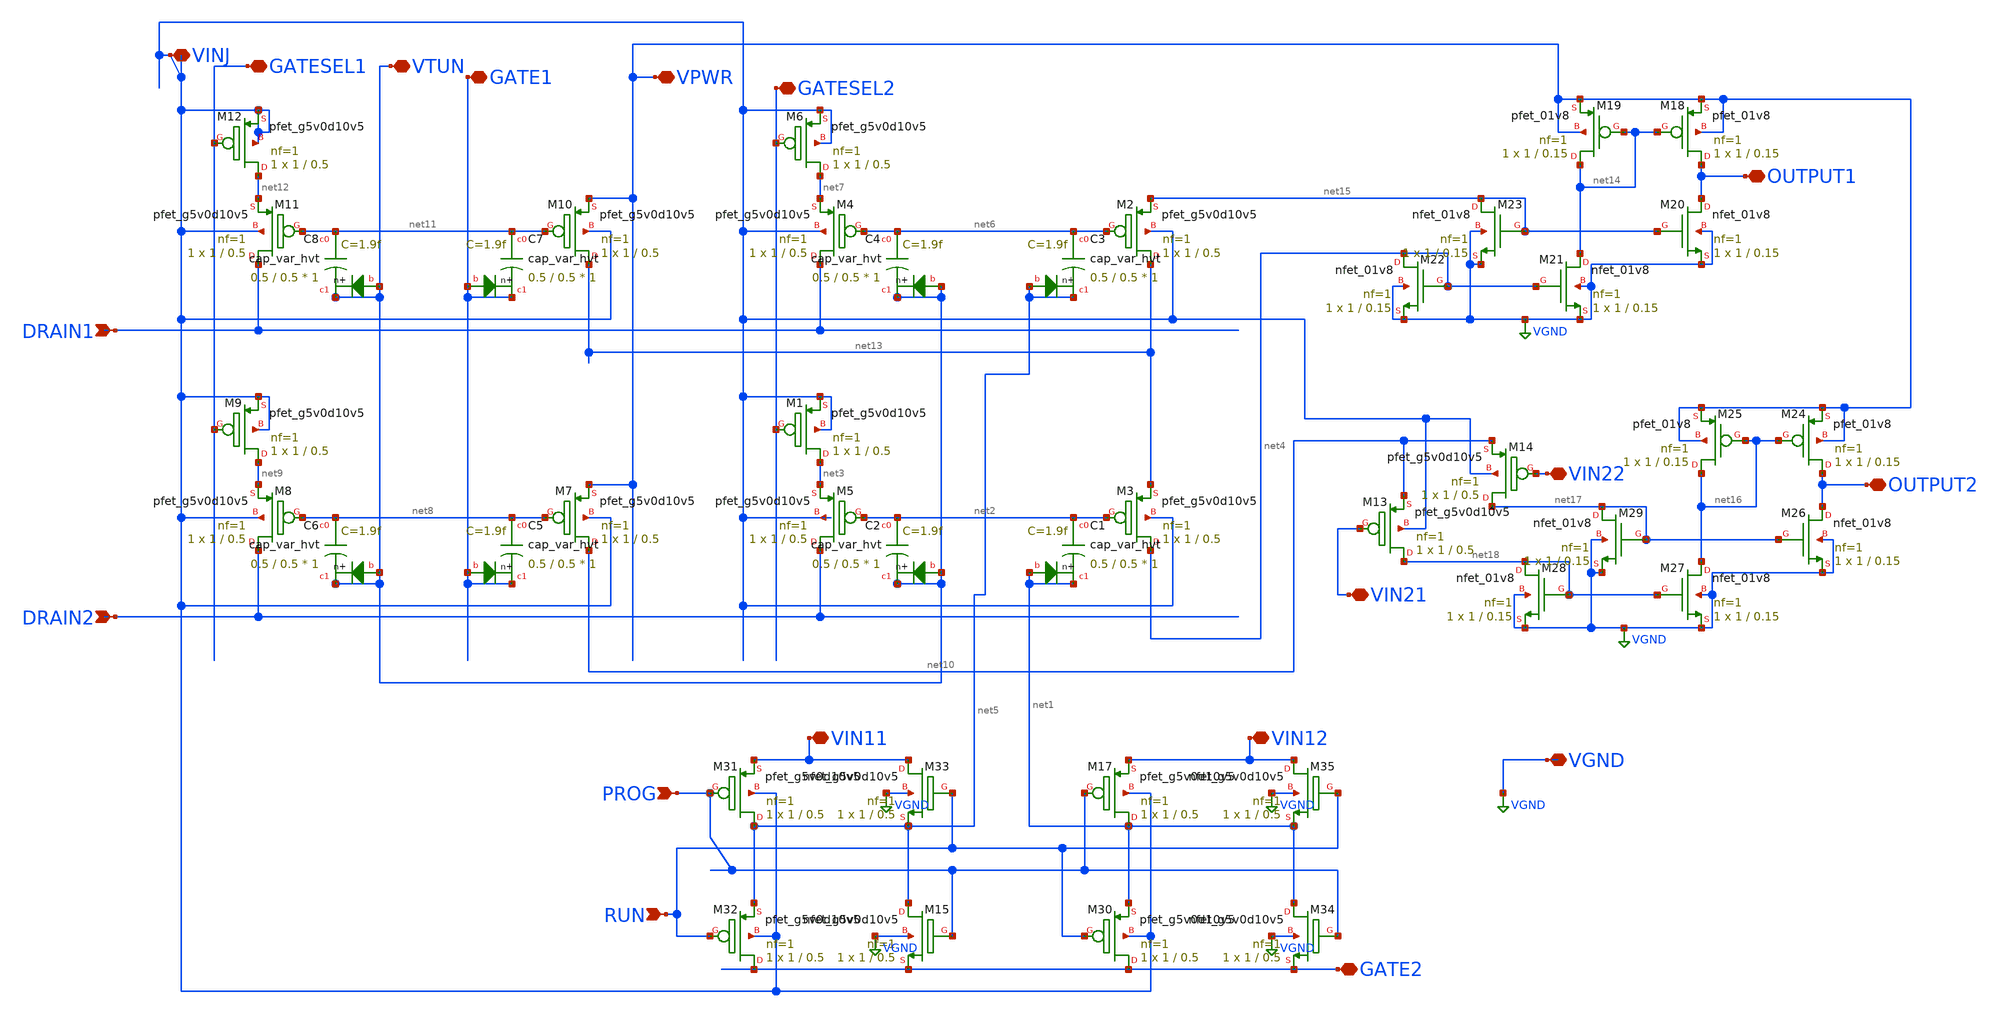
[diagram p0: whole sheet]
** sch_path: libs.ref/sky130_hilas_sc/xschem/sky130_hilas_TA2Cell_1FG_Strong.sch
**.subckt sky130_hilas_TA2Cell_1FG_Strong DRAIN1 DRAIN2 RUN PROG VPWR GATE1 VTUN GATESEL1 VINJ
*+ GATESEL2 GATE2 OUTPUT1 OUTPUT2 VIN11 VIN21 VIN12 VIN22 VGND
*.ipin DRAIN1
*.ipin DRAIN2
*.ipin RUN
*.ipin PROG
*.iopin VPWR
*.iopin GATE1
*.iopin VTUN
*.iopin GATESEL1
*.iopin VINJ
*.iopin GATESEL2
*.iopin GATE2
*.iopin OUTPUT1
*.iopin OUTPUT2
*.iopin VIN11
*.iopin VIN21
*.iopin VIN12
*.iopin VIN22
*.iopin VGND
XM3 net4 net2 net13 VINJ sky130_fd_pr__pfet_g5v0d10v5 L=0.5 W=1 nf=1 ad='int((nf+1)/2) * W/nf * 0.29'
+ as='int((nf+2)/2) * W/nf * 0.29' pd='2*int((nf+1)/2) * (W/nf + 0.29)' ps='2*int((nf+2)/2) * (W/nf + 0.29)'
+ nrd='0.29 / W' nrs='0.29 / W' sa=0 sb=0 sd=0 mult=1 m=1
XC1 net2 net1 net1 sky130_fd_pr__cap_var_hvt W=0.5 L=0.5 VM=1 m=1
XM5 DRAIN2 net2 net3 VINJ sky130_fd_pr__pfet_g5v0d10v5 L=0.5 W=1 nf=1 ad='int((nf+1)/2) * W/nf * 0.29'
+ as='int((nf+2)/2) * W/nf * 0.29' pd='2*int((nf+1)/2) * (W/nf + 0.29)' ps='2*int((nf+2)/2) * (W/nf + 0.29)'
+ nrd='0.29 / W' nrs='0.29 / W' sa=0 sb=0 sd=0 mult=1 m=1
XC2 net2 VTUN VTUN sky130_fd_pr__cap_var_hvt W=0.5 L=0.5 VM=1 m=1
XM1 net3 GATESEL2 VINJ VINJ sky130_fd_pr__pfet_g5v0d10v5 L=0.5 W=1 nf=1 ad='int((nf+1)/2) * W/nf * 0.29'
+ as='int((nf+2)/2) * W/nf * 0.29' pd='2*int((nf+1)/2) * (W/nf + 0.29)' ps='2*int((nf+2)/2) * (W/nf + 0.29)'
+ nrd='0.29 / W' nrs='0.29 / W' sa=0 sb=0 sd=0 mult=1 m=1
XM2 net13 net6 net15 VINJ sky130_fd_pr__pfet_g5v0d10v5 L=0.5 W=1 nf=1 ad='int((nf+1)/2) * W/nf * 0.29'
+ as='int((nf+2)/2) * W/nf * 0.29' pd='2*int((nf+1)/2) * (W/nf + 0.29)' ps='2*int((nf+2)/2) * (W/nf + 0.29)'
+ nrd='0.29 / W' nrs='0.29 / W' sa=0 sb=0 sd=0 mult=1 m=1
XC3 net6 net5 net5 sky130_fd_pr__cap_var_hvt W=0.5 L=0.5 VM=1 m=1
XM4 DRAIN1 net6 net7 VINJ sky130_fd_pr__pfet_g5v0d10v5 L=0.5 W=1 nf=1 ad='int((nf+1)/2) * W/nf * 0.29'
+ as='int((nf+2)/2) * W/nf * 0.29' pd='2*int((nf+1)/2) * (W/nf + 0.29)' ps='2*int((nf+2)/2) * (W/nf + 0.29)'
+ nrd='0.29 / W' nrs='0.29 / W' sa=0 sb=0 sd=0 mult=1 m=1
XC4 net6 VTUN VTUN sky130_fd_pr__cap_var_hvt W=0.5 L=0.5 VM=1 m=1
XM6 net7 GATESEL2 VINJ VINJ sky130_fd_pr__pfet_g5v0d10v5 L=0.5 W=1 nf=1 ad='int((nf+1)/2) * W/nf * 0.29'
+ as='int((nf+2)/2) * W/nf * 0.29' pd='2*int((nf+1)/2) * (W/nf + 0.29)' ps='2*int((nf+2)/2) * (W/nf + 0.29)'
+ nrd='0.29 / W' nrs='0.29 / W' sa=0 sb=0 sd=0 mult=1 m=1
XM7 net10 net8 VPWR VINJ sky130_fd_pr__pfet_g5v0d10v5 L=0.5 W=1 nf=1 ad='int((nf+1)/2) * W/nf * 0.29'
+ as='int((nf+2)/2) * W/nf * 0.29' pd='2*int((nf+1)/2) * (W/nf + 0.29)' ps='2*int((nf+2)/2) * (W/nf + 0.29)'
+ nrd='0.29 / W' nrs='0.29 / W' sa=0 sb=0 sd=0 mult=1 m=1
XC5 net8 GATE1 GATE1 sky130_fd_pr__cap_var_hvt W=0.5 L=0.5 VM=1 m=1
XM8 DRAIN2 net8 net9 VINJ sky130_fd_pr__pfet_g5v0d10v5 L=0.5 W=1 nf=1 ad='int((nf+1)/2) * W/nf * 0.29'
+ as='int((nf+2)/2) * W/nf * 0.29' pd='2*int((nf+1)/2) * (W/nf + 0.29)' ps='2*int((nf+2)/2) * (W/nf + 0.29)'
+ nrd='0.29 / W' nrs='0.29 / W' sa=0 sb=0 sd=0 mult=1 m=1
XC6 net8 VTUN VTUN sky130_fd_pr__cap_var_hvt W=0.5 L=0.5 VM=1 m=1
XM9 net9 GATESEL1 VINJ VINJ sky130_fd_pr__pfet_g5v0d10v5 L=0.5 W=1 nf=1 ad='int((nf+1)/2) * W/nf * 0.29'
+ as='int((nf+2)/2) * W/nf * 0.29' pd='2*int((nf+1)/2) * (W/nf + 0.29)' ps='2*int((nf+2)/2) * (W/nf + 0.29)'
+ nrd='0.29 / W' nrs='0.29 / W' sa=0 sb=0 sd=0 mult=1 m=1
XM10 net13 net11 VPWR VINJ sky130_fd_pr__pfet_g5v0d10v5 L=0.5 W=1 nf=1 ad='int((nf+1)/2) * W/nf * 0.29'
+ as='int((nf+2)/2) * W/nf * 0.29' pd='2*int((nf+1)/2) * (W/nf + 0.29)' ps='2*int((nf+2)/2) * (W/nf + 0.29)'
+ nrd='0.29 / W' nrs='0.29 / W' sa=0 sb=0 sd=0 mult=1 m=1
XC7 net11 GATE1 GATE1 sky130_fd_pr__cap_var_hvt W=0.5 L=0.5 VM=1 m=1
XM11 DRAIN1 net11 net12 VINJ sky130_fd_pr__pfet_g5v0d10v5 L=0.5 W=1 nf=1 ad='int((nf+1)/2) * W/nf * 0.29'
+ as='int((nf+2)/2) * W/nf * 0.29' pd='2*int((nf+1)/2) * (W/nf + 0.29)' ps='2*int((nf+2)/2) * (W/nf + 0.29)'
+ nrd='0.29 / W' nrs='0.29 / W' sa=0 sb=0 sd=0 mult=1 m=1
XC8 net11 VTUN VTUN sky130_fd_pr__cap_var_hvt W=0.5 L=0.5 VM=1 m=1
XM12 net12 GATESEL1 VINJ VINJ sky130_fd_pr__pfet_g5v0d10v5 L=0.5 W=1 nf=1 ad='int((nf+1)/2) * W/nf * 0.29'
+ as='int((nf+2)/2) * W/nf * 0.29' pd='2*int((nf+1)/2) * (W/nf + 0.29)' ps='2*int((nf+2)/2) * (W/nf + 0.29)'
+ nrd='0.29 / W' nrs='0.29 / W' sa=0 sb=0 sd=0 mult=1 m=1
XM15 net5 PROG GATE2 VGND sky130_fd_pr__nfet_g5v0d10v5 L=0.5 W=1 nf=1 ad='int((nf+1)/2) * W/nf * 0.29'
+ as='int((nf+2)/2) * W/nf * 0.29' pd='2*int((nf+1)/2) * (W/nf + 0.29)' ps='2*int((nf+2)/2) * (W/nf + 0.29)'
+ nrd='0.29 / W' nrs='0.29 / W' sa=0 sb=0 sd=0 mult=1 m=1
XM17 net1 PROG VIN12 VINJ sky130_fd_pr__pfet_g5v0d10v5 L=0.5 W=1 nf=1 ad='int((nf+1)/2) * W/nf * 0.29'
+ as='int((nf+2)/2) * W/nf * 0.29' pd='2*int((nf+1)/2) * (W/nf + 0.29)' ps='2*int((nf+2)/2) * (W/nf + 0.29)'
+ nrd='0.29 / W' nrs='0.29 / W' sa=0 sb=0 sd=0 mult=1 m=1
XM18 OUTPUT1 net14 VPWR VPWR sky130_fd_pr__pfet_01v8 L=0.15 W=1 nf=1 ad='int((nf+1)/2) * W/nf * 0.29'
+ as='int((nf+2)/2) * W/nf * 0.29' pd='2*int((nf+1)/2) * (W/nf + 0.29)' ps='2*int((nf+2)/2) * (W/nf + 0.29)'
+ nrd='0.29 / W' nrs='0.29 / W' sa=0 sb=0 sd=0 mult=1 m=1
XM19 net14 net14 VPWR VPWR sky130_fd_pr__pfet_01v8 L=0.15 W=1 nf=1 ad='int((nf+1)/2) * W/nf * 0.29' as='int((nf+2)/2) * W/nf * 0.29'
+ pd='2*int((nf+1)/2) * (W/nf + 0.29)' ps='2*int((nf+2)/2) * (W/nf + 0.29)' nrd='0.29 / W' nrs='0.29 / W'
+ sa=0 sb=0 sd=0 mult=1 m=1
XM20 OUTPUT1 net15 VGND VGND sky130_fd_pr__nfet_01v8 L=0.15 W=1 nf=1 ad='int((nf+1)/2) * W/nf * 0.29'
+ as='int((nf+2)/2) * W/nf * 0.29' pd='2*int((nf+1)/2) * (W/nf + 0.29)' ps='2*int((nf+2)/2) * (W/nf + 0.29)'
+ nrd='0.29 / W' nrs='0.29 / W' sa=0 sb=0 sd=0 mult=1 m=1
XM21 net14 net4 VGND VGND sky130_fd_pr__nfet_01v8 L=0.15 W=1 nf=1 ad='int((nf+1)/2) * W/nf * 0.29' as='int((nf+2)/2) * W/nf * 0.29'
+ pd='2*int((nf+1)/2) * (W/nf + 0.29)' ps='2*int((nf+2)/2) * (W/nf + 0.29)' nrd='0.29 / W' nrs='0.29 / W'
+ sa=0 sb=0 sd=0 mult=1 m=1
XM22 net4 net4 VGND VGND sky130_fd_pr__nfet_01v8 L=0.15 W=1 nf=1 ad='int((nf+1)/2) * W/nf * 0.29' as='int((nf+2)/2) * W/nf * 0.29'
+ pd='2*int((nf+1)/2) * (W/nf + 0.29)' ps='2*int((nf+2)/2) * (W/nf + 0.29)' nrd='0.29 / W' nrs='0.29 / W'
+ sa=0 sb=0 sd=0 mult=1 m=1
XM23 net15 net15 VGND VGND sky130_fd_pr__nfet_01v8 L=0.15 W=1 nf=1 ad='int((nf+1)/2) * W/nf * 0.29' as='int((nf+2)/2) * W/nf * 0.29'
+ pd='2*int((nf+1)/2) * (W/nf + 0.29)' ps='2*int((nf+2)/2) * (W/nf + 0.29)' nrd='0.29 / W' nrs='0.29 / W'
+ sa=0 sb=0 sd=0 mult=1 m=1
XM24 OUTPUT2 net16 VPWR VPWR sky130_fd_pr__pfet_01v8 L=0.15 W=1 nf=1 ad='int((nf+1)/2) * W/nf * 0.29'
+ as='int((nf+2)/2) * W/nf * 0.29' pd='2*int((nf+1)/2) * (W/nf + 0.29)' ps='2*int((nf+2)/2) * (W/nf + 0.29)'
+ nrd='0.29 / W' nrs='0.29 / W' sa=0 sb=0 sd=0 mult=1 m=1
XM25 net16 net16 VPWR VPWR sky130_fd_pr__pfet_01v8 L=0.15 W=1 nf=1 ad='int((nf+1)/2) * W/nf * 0.29' as='int((nf+2)/2) * W/nf * 0.29'
+ pd='2*int((nf+1)/2) * (W/nf + 0.29)' ps='2*int((nf+2)/2) * (W/nf + 0.29)' nrd='0.29 / W' nrs='0.29 / W'
+ sa=0 sb=0 sd=0 mult=1 m=1
XM26 OUTPUT2 net17 VGND VGND sky130_fd_pr__nfet_01v8 L=0.15 W=1 nf=1 ad='int((nf+1)/2) * W/nf * 0.29'
+ as='int((nf+2)/2) * W/nf * 0.29' pd='2*int((nf+1)/2) * (W/nf + 0.29)' ps='2*int((nf+2)/2) * (W/nf + 0.29)'
+ nrd='0.29 / W' nrs='0.29 / W' sa=0 sb=0 sd=0 mult=1 m=1
XM27 net16 net18 VGND VGND sky130_fd_pr__nfet_01v8 L=0.15 W=1 nf=1 ad='int((nf+1)/2) * W/nf * 0.29' as='int((nf+2)/2) * W/nf * 0.29'
+ pd='2*int((nf+1)/2) * (W/nf + 0.29)' ps='2*int((nf+2)/2) * (W/nf + 0.29)' nrd='0.29 / W' nrs='0.29 / W'
+ sa=0 sb=0 sd=0 mult=1 m=1
XM28 net18 net18 VGND VGND sky130_fd_pr__nfet_01v8 L=0.15 W=1 nf=1 ad='int((nf+1)/2) * W/nf * 0.29' as='int((nf+2)/2) * W/nf * 0.29'
+ pd='2*int((nf+1)/2) * (W/nf + 0.29)' ps='2*int((nf+2)/2) * (W/nf + 0.29)' nrd='0.29 / W' nrs='0.29 / W'
+ sa=0 sb=0 sd=0 mult=1 m=1
XM29 net17 net17 VGND VGND sky130_fd_pr__nfet_01v8 L=0.15 W=1 nf=1 ad='int((nf+1)/2) * W/nf * 0.29' as='int((nf+2)/2) * W/nf * 0.29'
+ pd='2*int((nf+1)/2) * (W/nf + 0.29)' ps='2*int((nf+2)/2) * (W/nf + 0.29)' nrd='0.29 / W' nrs='0.29 / W'
+ sa=0 sb=0 sd=0 mult=1 m=1
XM30 GATE2 RUN net1 VINJ sky130_fd_pr__pfet_g5v0d10v5 L=0.5 W=1 nf=1 ad='int((nf+1)/2) * W/nf * 0.29'
+ as='int((nf+2)/2) * W/nf * 0.29' pd='2*int((nf+1)/2) * (W/nf + 0.29)' ps='2*int((nf+2)/2) * (W/nf + 0.29)'
+ nrd='0.29 / W' nrs='0.29 / W' sa=0 sb=0 sd=0 mult=1 m=1
XM31 net5 PROG VIN11 VINJ sky130_fd_pr__pfet_g5v0d10v5 L=0.5 W=1 nf=1 ad='int((nf+1)/2) * W/nf * 0.29'
+ as='int((nf+2)/2) * W/nf * 0.29' pd='2*int((nf+1)/2) * (W/nf + 0.29)' ps='2*int((nf+2)/2) * (W/nf + 0.29)'
+ nrd='0.29 / W' nrs='0.29 / W' sa=0 sb=0 sd=0 mult=1 m=1
XM32 GATE2 RUN net5 VINJ sky130_fd_pr__pfet_g5v0d10v5 L=0.5 W=1 nf=1 ad='int((nf+1)/2) * W/nf * 0.29'
+ as='int((nf+2)/2) * W/nf * 0.29' pd='2*int((nf+1)/2) * (W/nf + 0.29)' ps='2*int((nf+2)/2) * (W/nf + 0.29)'
+ nrd='0.29 / W' nrs='0.29 / W' sa=0 sb=0 sd=0 mult=1 m=1
XM33 VIN11 RUN net5 VGND sky130_fd_pr__nfet_g5v0d10v5 L=0.5 W=1 nf=1 ad='int((nf+1)/2) * W/nf * 0.29'
+ as='int((nf+2)/2) * W/nf * 0.29' pd='2*int((nf+1)/2) * (W/nf + 0.29)' ps='2*int((nf+2)/2) * (W/nf + 0.29)'
+ nrd='0.29 / W' nrs='0.29 / W' sa=0 sb=0 sd=0 mult=1 m=1
XM34 net1 PROG GATE2 VGND sky130_fd_pr__nfet_g5v0d10v5 L=0.5 W=1 nf=1 ad='int((nf+1)/2) * W/nf * 0.29'
+ as='int((nf+2)/2) * W/nf * 0.29' pd='2*int((nf+1)/2) * (W/nf + 0.29)' ps='2*int((nf+2)/2) * (W/nf + 0.29)'
+ nrd='0.29 / W' nrs='0.29 / W' sa=0 sb=0 sd=0 mult=1 m=1
XM35 VIN12 RUN net1 VGND sky130_fd_pr__nfet_g5v0d10v5 L=0.5 W=1 nf=1 ad='int((nf+1)/2) * W/nf * 0.29'
+ as='int((nf+2)/2) * W/nf * 0.29' pd='2*int((nf+1)/2) * (W/nf + 0.29)' ps='2*int((nf+2)/2) * (W/nf + 0.29)'
+ nrd='0.29 / W' nrs='0.29 / W' sa=0 sb=0 sd=0 mult=1 m=1
XM13 net18 VIN21 net10 VINJ sky130_fd_pr__pfet_g5v0d10v5 L=0.5 W=1 nf=1 ad='int((nf+1)/2) * W/nf * 0.29'
+ as='int((nf+2)/2) * W/nf * 0.29' pd='2*int((nf+1)/2) * (W/nf + 0.29)' ps='2*int((nf+2)/2) * (W/nf + 0.29)'
+ nrd='0.29 / W' nrs='0.29 / W' sa=0 sb=0 sd=0 mult=1 m=1
XM14 net17 VIN22 net10 VINJ sky130_fd_pr__pfet_g5v0d10v5 L=0.5 W=1 nf=1 ad='int((nf+1)/2) * W/nf * 0.29'
+ as='int((nf+2)/2) * W/nf * 0.29' pd='2*int((nf+1)/2) * (W/nf + 0.29)' ps='2*int((nf+2)/2) * (W/nf + 0.29)'
+ nrd='0.29 / W' nrs='0.29 / W' sa=0 sb=0 sd=0 mult=1 m=1
**.ends
.GLOBAL VGND
.end
